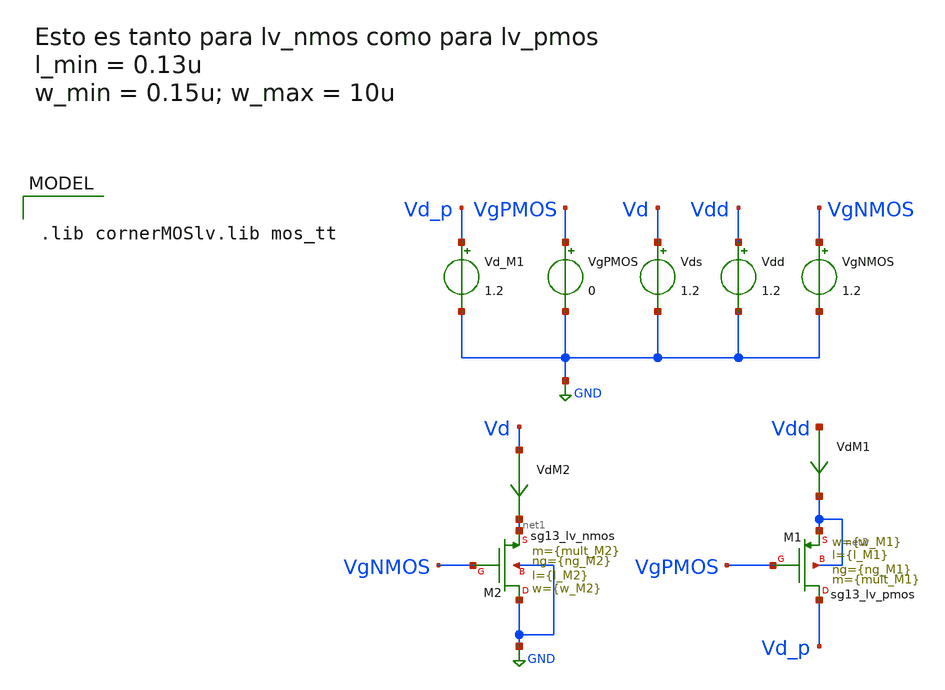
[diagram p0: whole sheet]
** sch_path: ChipUSM_AnalogTrack24/TestBenchs/TB_lvMOS_Comp.sch
**.subckt TB_lvMOS_Comp
VgPMOS VgPMOS GND 0
Vds Vd GND 1.2
Vdd Vdd GND 1.2
VdM1 Vdd net2 0
.save i(vdm1)
VdM2 Vd net1 0
.save i(vdm2)
Vd_M1 Vd_p GND 1.2
XM2 GND VgNMOS net1 GND sg13_lv_nmos w={w_M2} l={l_M2} ng={ng_M2} m={mult_M2} mm_ok=1
XM1 Vd_p VgPMOS net2 net2 sg13_lv_pmos w={w_M1} l={l_M1} ng={ng_M1} m={mult_M1} mm_ok=1
VgNMOS VgNMOS GND 1.2
**** begin user architecture code

.lib cornerMOSlv.lib mos_tt



.save all  @n.xm1.nsg13_lv_pmos[vth]  @n.xm1.nsg13_lv_pmos[gds]  @n.xm1.nsg13_lv_pmos[ad]  @n.xm2.nsg13_lv_nmos[vth]  @n.xm2.nsg13_lv_nmos[gds]

.control
reset
*alter Vg 1.2
dc Vds 0 1.2 0.01
*dc Vds 0 0.5 0.01 temp 0 27 1
let Vds_M2 = v(Vd)


let G_M2 = @n.xm2.nsg13_lv_nmos[gds]
let Ron_M2 = 1/G_M2
let I_M2 = i(VdM2)
let G_M22 = deriv(I_M2)
let Ron_M22 = 1/G_M22

plot Ron_M2 vs Vds_M2
plot i(VdM2) vs Vds_M2

*let VthM1_off =  @n.xm1.nsg13_hv_pmos[vth]
*let VthM2 =  @n.xm2.nsg13_hv_nmos[vth]
*plot VthM1_off
*plot VthM2
.endc

.control
reset
*alter Vg 0
dc Vd_M1 0 1.2 0.01
*dc Vd_M1 2 3.3 0.01 temp 0 27 1

let Vsd_M1 = v(Vdd) -v(Vd_p)
plot i(VdM1) vs Vsd_M1
let G_M1 = @n.xm1.nsg13_lv_pmos[gds]
let Ron_M1 = 1/G_M1
let I_M1 = i(VdM1)
let G_M11 = deriv(I_M1)
let Ron_M11 = -1/G_M11

plot Ron_M1 vs Vsd_M1

*plot Ron_M11
*plot Ron_M11 vs Vsd_M1
*let VthM1_on = @n.xm1.nsg13_lv_pmos[vth]
*plot VthM1_on
.endc

.control
reset
*alter Vg 1.2
dc Vd_M1 0 1.2 0.01
let Vsd_M1 = v(Vdd) -v(Vd_p)
*plot i(VdM1) vs Vsd_M1
let G_M1 = @n.xm1.nsg13_lv_pmos[gds]
let I_M1 = i(VdM1)


let VthM1_subth = @n.xm1.nsg13_lv_pmos[vth]
*plot VthM1_subth
.endc
.end




.param temp=27
.param mult_M1 = 2
.param w_M1 = 0.15u
.param l_M1 = 0.13u
.param ng_M1 = 1

.param mult_M2 = 1
.param w_M2 =0.15u
.param l_M2 =0.13u
.param ng_M2 =1





**** end user architecture code
**.ends
.GLOBAL GND
.end
